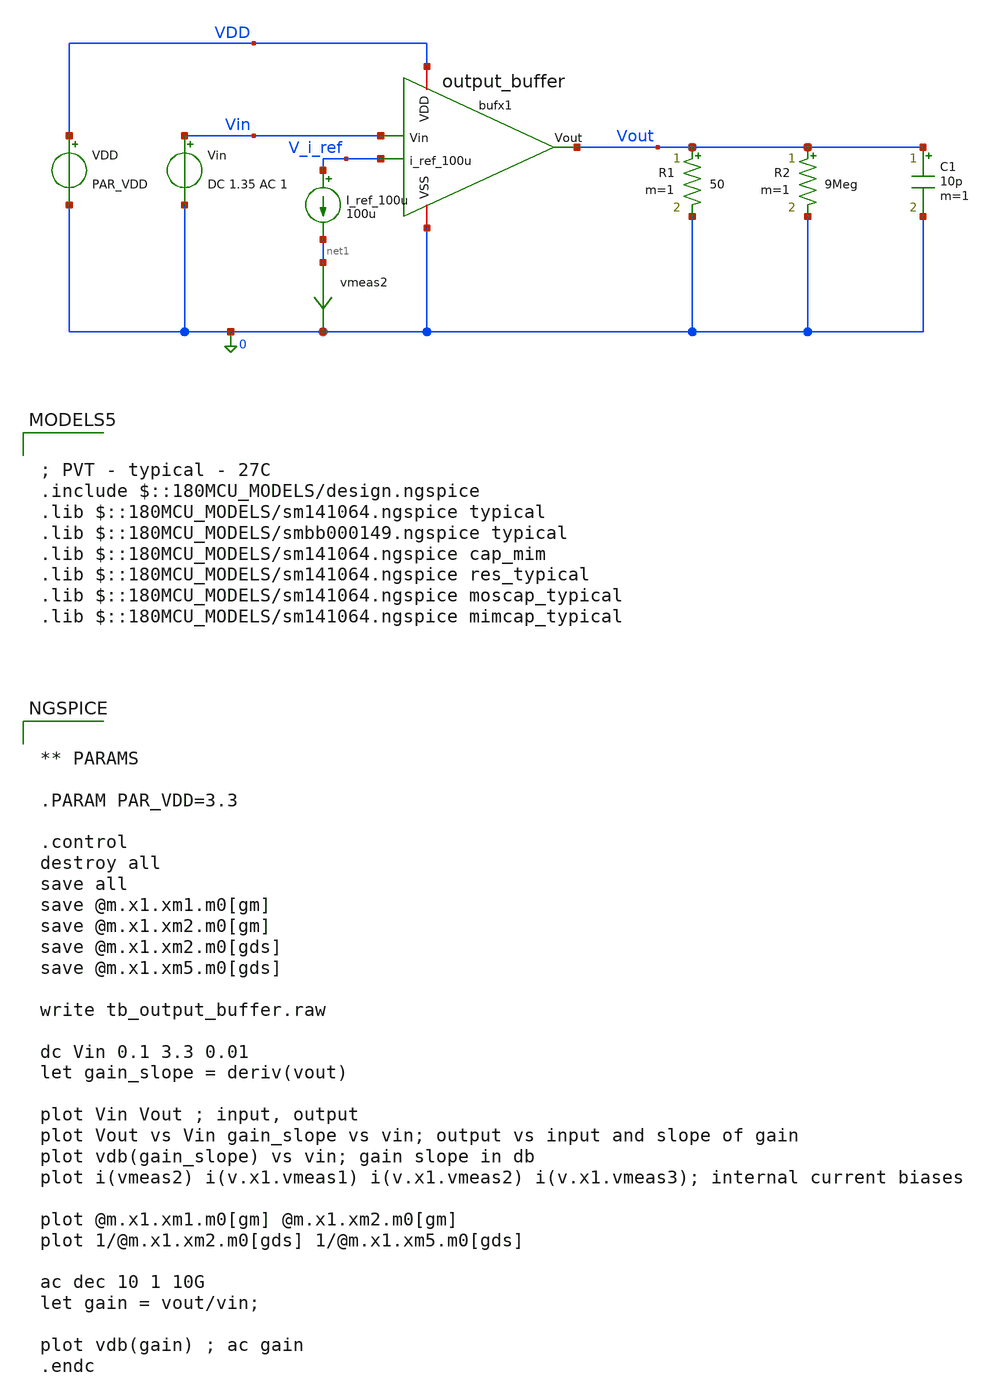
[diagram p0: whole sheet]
** sch_path: designs/output_buffer/testbench/tb_output_buffer_nfet_input.sch
**.subckt tb_output_buffer_nfet_input
x1 Vout Vin V_i_ref VDD 0 output_buffer
I_ref_100u V_i_ref net1 100u
Vin Vin 0 DC 1.35 AC 1
VDD VDD 0 PAR_VDD
R1 Vout 0 50 m=1
vmeas2 net1 0 0
.save i(vmeas2)
R2 Vout 0 9Meg m=1
C1 Vout 0 10p m=1
**** begin user architecture code

; PVT - typical - 27C
.include $::180MCU_MODELS/design.ngspice
.lib $::180MCU_MODELS/sm141064.ngspice typical
.lib $::180MCU_MODELS/smbb000149.ngspice typical
.lib $::180MCU_MODELS/sm141064.ngspice cap_mim
.lib $::180MCU_MODELS/sm141064.ngspice res_typical
.lib $::180MCU_MODELS/sm141064.ngspice moscap_typical
.lib $::180MCU_MODELS/sm141064.ngspice mimcap_typical



** PARAMS

.PARAM PAR_VDD=3.3

.control
destroy all
save all
save @m.x1.xm1.m0[gm]
save @m.x1.xm2.m0[gm]
save @m.x1.xm2.m0[gds]
save @m.x1.xm5.m0[gds]

write tb_output_buffer.raw

dc Vin 0.1 3.3 0.01
let gain_slope = deriv(vout)

plot Vin Vout ; input, output
plot Vout vs Vin gain_slope vs vin; output vs input and slope of gain
plot vdb(gain_slope) vs vin; gain slope in db
plot i(vmeas2) i(v.x1.vmeas1) i(v.x1.vmeas2) i(v.x1.vmeas3); internal current biases

plot @m.x1.xm1.m0[gm] @m.x1.xm2.m0[gm]
plot 1/@m.x1.xm2.m0[gds] 1/@m.x1.xm5.m0[gds]

ac dec 10 1 10G
let gain = vout/vin;

plot vdb(gain) ; ac gain
.endc


**** end user architecture code
**.ends

* expanding   symbol:  output_buffer/schematic/output_buffer.sym # of pins=5
** sym_path: designs/output_buffer/schematic/output_buffer.sym
** sch_path: designs/output_buffer/schematic/output_buffer.sch
.subckt output_buffer Vout Vin i_ref_100u VDD VSS
*.ipin Vin
*.opin Vout
*.ipin i_ref_100u
*.iopin VDD
*.iopin VSS
XM1 net1 Vin net2 VSS nfet_03v3 L=0.28u W=45u nf=8 ad='int((nf+1)/2) * W/nf * 0.18u' as='int((nf+2)/2) * W/nf * 0.18u'
+ pd='2*int((nf+1)/2) * (W/nf + 0.18u)' ps='2*int((nf+2)/2) * (W/nf + 0.18u)' nrd='0.18u / W' nrs='0.18u / W'
+ sa=0 sb=0 sd=0 m=1
XM2 net4 net1 VDD VDD pfet_03v3 L=0.28u W=40u nf=10 ad='int((nf+1)/2) * W/nf * 0.18u' as='int((nf+2)/2) * W/nf * 0.18u'
+ pd='2*int((nf+1)/2) * (W/nf + 0.18u)' ps='2*int((nf+2)/2) * (W/nf + 0.18u)' nrd='0.18u / W' nrs='0.18u / W'
+ sa=0 sb=0 sd=0 m=1
XM3 net1 i_ref_100u VDD VDD pfet_03v3 L=0.5u W=80u nf=10 ad='int((nf+1)/2) * W/nf * 0.18u' as='int((nf+2)/2) * W/nf * 0.18u'
+ pd='2*int((nf+1)/2) * (W/nf + 0.18u)' ps='2*int((nf+2)/2) * (W/nf + 0.18u)' nrd='0.18u / W' nrs='0.18u / W'
+ sa=0 sb=0 sd=0 m=1
XM4 i_ref_100u i_ref_100u VDD VDD pfet_03v3 L=.5u W=4u nf=1 ad='int((nf+1)/2) * W/nf * 0.18u' as='int((nf+2)/2) * W/nf * 0.18u'
+ pd='2*int((nf+1)/2) * (W/nf + 0.18u)' ps='2*int((nf+2)/2) * (W/nf + 0.18u)' nrd='0.18u / W' nrs='0.18u / W'
+ sa=0 sb=0 sd=0 m=1
XM5 net6 net5 VSS VSS nfet_03v3 L=.5u W=20u nf=10 ad='int((nf+1)/2) * W/nf * 0.18u' as='int((nf+2)/2) * W/nf * 0.18u'
+ pd='2*int((nf+1)/2) * (W/nf + 0.18u)' ps='2*int((nf+2)/2) * (W/nf + 0.18u)' nrd='0.18u / W' nrs='0.18u / W'
+ sa=0 sb=0 sd=0 m=1
vmeas2 net4 Vout 0
.save i(vmeas2)
Vmeas1 Vout net6 0
.save i(vmeas1)
C1 net1 net5 1p m=1
XM6 net3 i_ref_100u VDD VDD pfet_03v3 L=0.5u W=16u nf=1 ad='int((nf+1)/2) * W/nf * 0.18u' as='int((nf+2)/2) * W/nf * 0.18u'
+ pd='2*int((nf+1)/2) * (W/nf + 0.18u)' ps='2*int((nf+2)/2) * (W/nf + 0.18u)' nrd='0.18u / W' nrs='0.18u / W'
+ sa=0 sb=0 sd=0 m=1
XM7 net3 net3 VSS VSS nfet_03v3 L=0.5u W=4u nf=1 ad='int((nf+1)/2) * W/nf * 0.18u' as='int((nf+2)/2) * W/nf * 0.18u'
+ pd='2*int((nf+1)/2) * (W/nf + 0.18u)' ps='2*int((nf+2)/2) * (W/nf + 0.18u)' nrd='0.18u / W' nrs='0.18u / W'
+ sa=0 sb=0 sd=0 m=1
Vmeas3 net2 Vout 0
.save i(vmeas3)
XM8 net6 net5 VSS VSS nfet_03v3 L=.5u W=80u nf=10 ad='int((nf+1)/2) * W/nf * 0.18u' as='int((nf+2)/2) * W/nf * 0.18u'
+ pd='2*int((nf+1)/2) * (W/nf + 0.18u)' ps='2*int((nf+2)/2) * (W/nf + 0.18u)' nrd='0.18u / W' nrs='0.18u / W'
+ sa=0 sb=0 sd=0 m=1
XM9 net7 net3 net3 VSS nfet_03v3 L=0.28u W=0.22u nf=1 ad='int((nf+1)/2) * W/nf * 0.18u' as='int((nf+2)/2) * W/nf * 0.18u'
+ pd='2*int((nf+1)/2) * (W/nf + 0.18u)' ps='2*int((nf+2)/2) * (W/nf + 0.18u)' nrd='0.18u / W' nrs='0.18u / W'
+ sa=0 sb=0 sd=0 m=1
XM10 net5 net7 net7 VSS nfet_03v3 L=0.28u W=0.22u nf=1 ad='int((nf+1)/2) * W/nf * 0.18u' as='int((nf+2)/2) * W/nf * 0.18u'
+ pd='2*int((nf+1)/2) * (W/nf + 0.18u)' ps='2*int((nf+2)/2) * (W/nf + 0.18u)' nrd='0.18u / W' nrs='0.18u / W'
+ sa=0 sb=0 sd=0 m=1
C2 net2 Vin 5p m=1
.ends

.end
